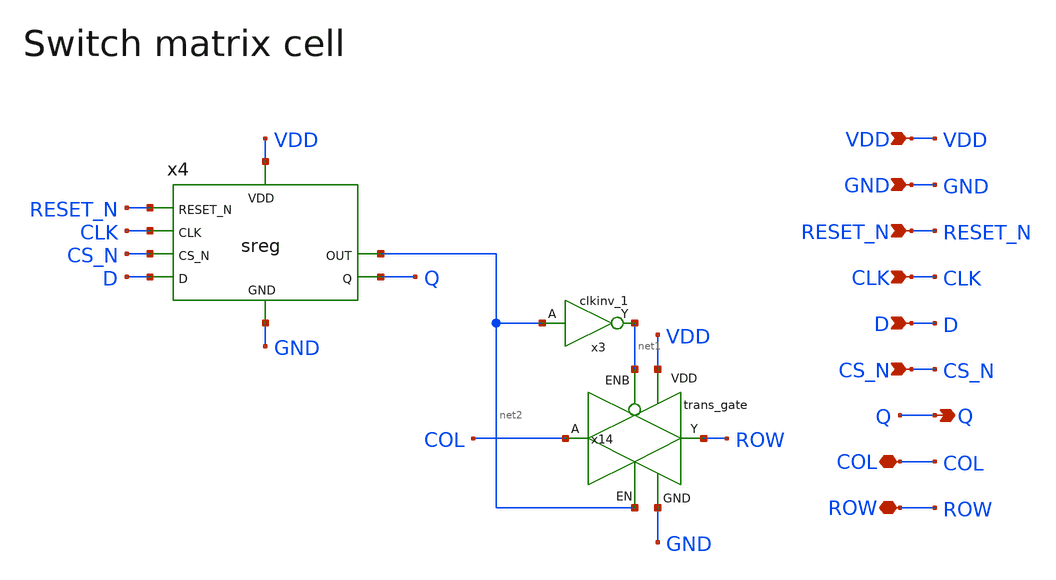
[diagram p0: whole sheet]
** sch_path: designs/libs/core_analog/sw_matrix/sw_matrix_cell.sch
* Copyright 2022 GlobalFoundries PDK Authors
* Licensed under the Apache License, Version 2.0 (the "License");
* you may not use this file except in compliance with the License.
* You may obtain a copy of the License at
* https://www.apache.org/licenses/LICENSE-2.0
* Unless required by applicable law or agreed to in writing, software
* distributed under the License is distributed on an "AS IS" BASIS,
* WITHOUT WARRANTIES OR CONDITIONS OF ANY KIND, either express or implied.
* See the License for the specific language governing permissions and
* limitations under the License.
**.subckt sw_matrix_cell RESET_N CLK D CS_N GND VDD Q COL ROW
*.ipin RESET_N
*.ipin CLK
*.ipin D
*.ipin CS_N
*.ipin GND
*.ipin VDD
*.opin Q
*.iopin COL
*.iopin ROW
x14 VDD GND COL net1 ROW net2 trans_gate
x3 net2 net1 VDD VDD GND GND gf180mcu_fd_sc_mcu7t5v0__clkinv_1
x4 VDD GND RESET_N CLK D CS_N Q net2 sreg
**.ends
.end
